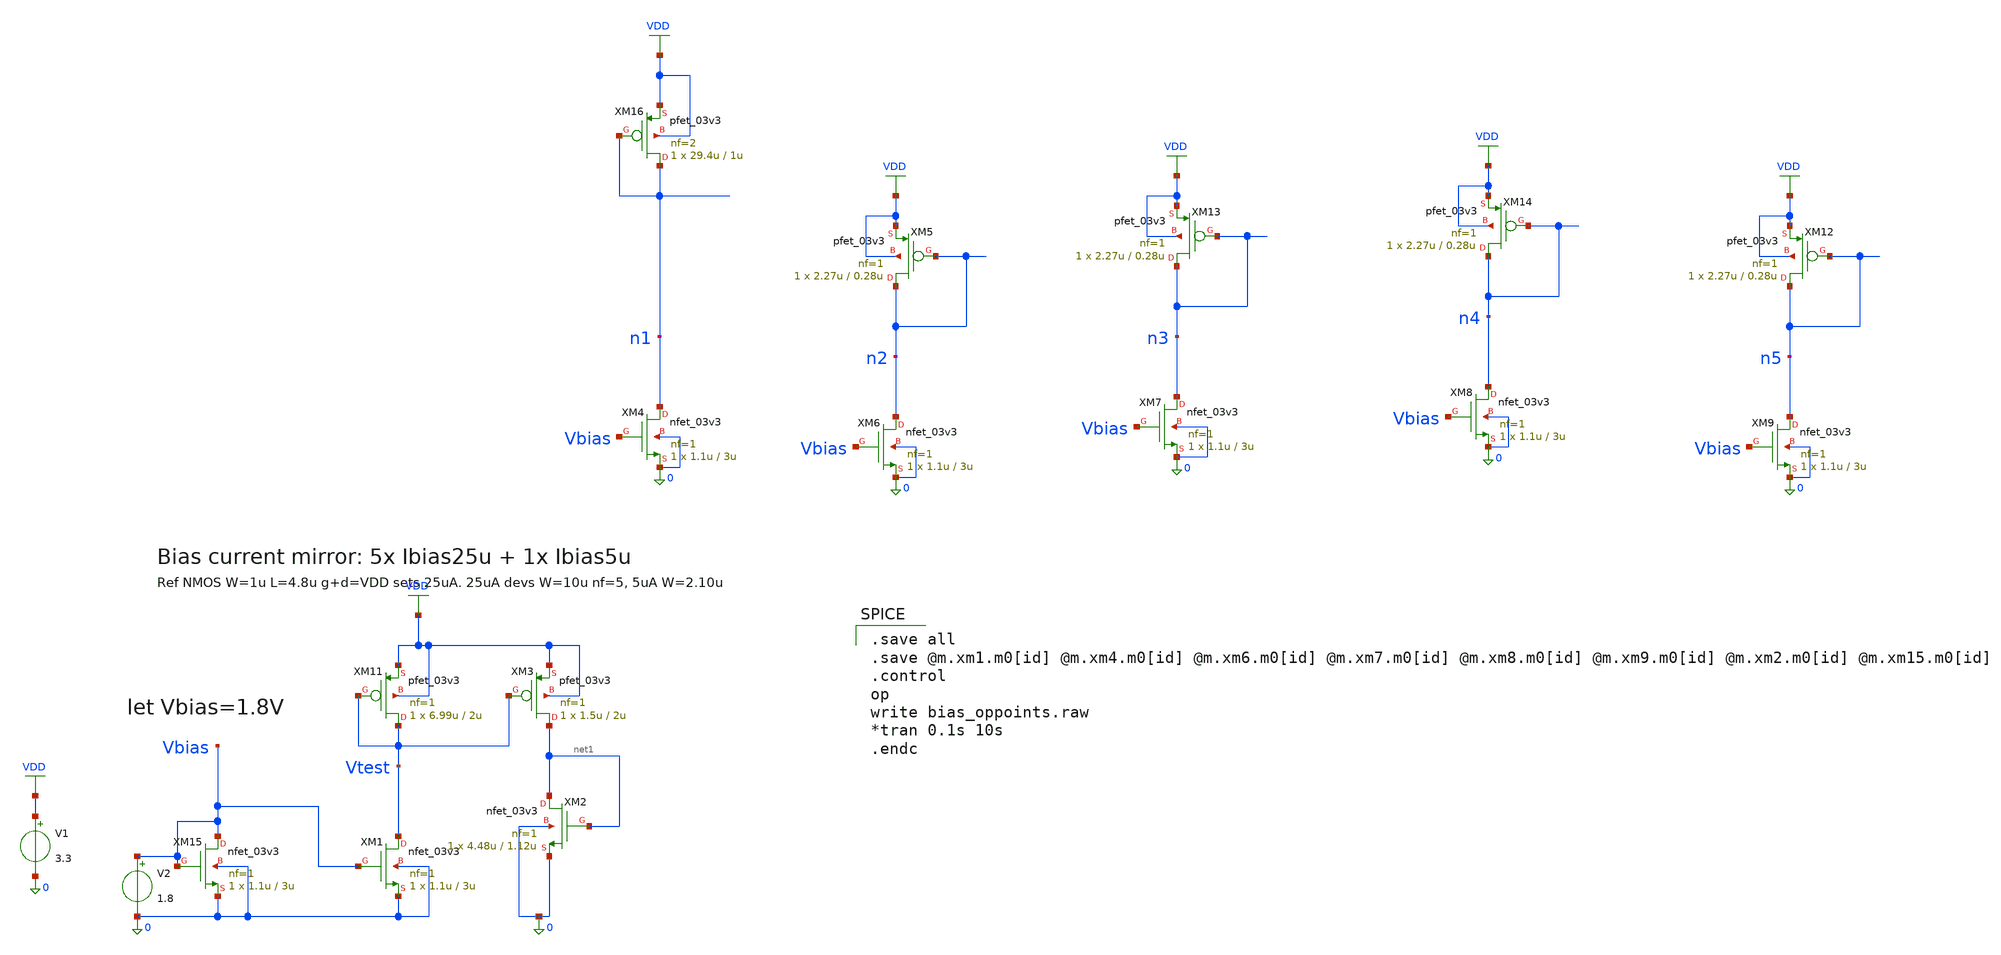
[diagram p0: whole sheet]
** sch_path: ps-bias/jz_bias_tb.sch
**.subckt jz_bias_tb
V1 VDD 0 3.3
V2 Vbias 0 1.8
XM5 n2 n2 VDD VDD pfet_03v3 L=0.28u W=2.27u nf=1 ad='int((nf+1)/2) * W/nf * 0.18u' as='int((nf+2)/2) * W/nf * 0.18u'
+ pd='2*int((nf+1)/2) * (W/nf + 0.18u)' ps='2*int((nf+2)/2) * (W/nf + 0.18u)' nrd='0.18u / W' nrs='0.18u / W'
+ sa=0 sb=0 sd=0 m=1
XM13 n3 n3 VDD VDD pfet_03v3 L=0.28u W=2.27u nf=1 ad='int((nf+1)/2) * W/nf * 0.18u' as='int((nf+2)/2) * W/nf * 0.18u'
+ pd='2*int((nf+1)/2) * (W/nf + 0.18u)' ps='2*int((nf+2)/2) * (W/nf + 0.18u)' nrd='0.18u / W' nrs='0.18u / W'
+ sa=0 sb=0 sd=0 m=1
XM14 n4 n4 VDD VDD pfet_03v3 L=0.28u W=2.27u nf=1 ad='int((nf+1)/2) * W/nf * 0.18u' as='int((nf+2)/2) * W/nf * 0.18u'
+ pd='2*int((nf+1)/2) * (W/nf + 0.18u)' ps='2*int((nf+2)/2) * (W/nf + 0.18u)' nrd='0.18u / W' nrs='0.18u / W'
+ sa=0 sb=0 sd=0 m=1
XM12 n5 n5 VDD VDD pfet_03v3 L=0.28u W=2.27u nf=1 ad='int((nf+1)/2) * W/nf * 0.18u' as='int((nf+2)/2) * W/nf * 0.18u'
+ pd='2*int((nf+1)/2) * (W/nf + 0.18u)' ps='2*int((nf+2)/2) * (W/nf + 0.18u)' nrd='0.18u / W' nrs='0.18u / W'
+ sa=0 sb=0 sd=0 m=1
XM15 Vbias Vbias 0 0 nfet_03v3 L=3u W=1.1u nf=1 ad='int((nf+1)/2) * W/nf * 0.18u' as='int((nf+2)/2) * W/nf * 0.18u'
+ pd='2*int((nf+1)/2) * (W/nf + 0.18u)' ps='2*int((nf+2)/2) * (W/nf + 0.18u)' nrd='0.18u / W' nrs='0.18u / W'
+ sa=0 sb=0 sd=0 m=1
XM1 Vtest Vbias 0 0 nfet_03v3 L=3u W=1.1u nf=1 ad='int((nf+1)/2) * W/nf * 0.18u' as='int((nf+2)/2) * W/nf * 0.18u'
+ pd='2*int((nf+1)/2) * (W/nf + 0.18u)' ps='2*int((nf+2)/2) * (W/nf + 0.18u)' nrd='0.18u / W' nrs='0.18u / W'
+ sa=0 sb=0 sd=0 m=1
XM4 n1 Vbias 0 0 nfet_03v3 L=3u W=1.1u nf=1 ad='int((nf+1)/2) * W/nf * 0.18u' as='int((nf+2)/2) * W/nf * 0.18u'
+ pd='2*int((nf+1)/2) * (W/nf + 0.18u)' ps='2*int((nf+2)/2) * (W/nf + 0.18u)' nrd='0.18u / W' nrs='0.18u / W'
+ sa=0 sb=0 sd=0 m=1
XM6 n2 Vbias 0 0 nfet_03v3 L=3u W=1.1u nf=1 ad='int((nf+1)/2) * W/nf * 0.18u' as='int((nf+2)/2) * W/nf * 0.18u'
+ pd='2*int((nf+1)/2) * (W/nf + 0.18u)' ps='2*int((nf+2)/2) * (W/nf + 0.18u)' nrd='0.18u / W' nrs='0.18u / W'
+ sa=0 sb=0 sd=0 m=1
XM7 n3 Vbias 0 0 nfet_03v3 L=3u W=1.1u nf=1 ad='int((nf+1)/2) * W/nf * 0.18u' as='int((nf+2)/2) * W/nf * 0.18u'
+ pd='2*int((nf+1)/2) * (W/nf + 0.18u)' ps='2*int((nf+2)/2) * (W/nf + 0.18u)' nrd='0.18u / W' nrs='0.18u / W'
+ sa=0 sb=0 sd=0 m=1
XM8 n4 Vbias 0 0 nfet_03v3 L=3u W=1.1u nf=1 ad='int((nf+1)/2) * W/nf * 0.18u' as='int((nf+2)/2) * W/nf * 0.18u'
+ pd='2*int((nf+1)/2) * (W/nf + 0.18u)' ps='2*int((nf+2)/2) * (W/nf + 0.18u)' nrd='0.18u / W' nrs='0.18u / W'
+ sa=0 sb=0 sd=0 m=1
XM9 n5 Vbias 0 0 nfet_03v3 L=3u W=1.1u nf=1 ad='int((nf+1)/2) * W/nf * 0.18u' as='int((nf+2)/2) * W/nf * 0.18u'
+ pd='2*int((nf+1)/2) * (W/nf + 0.18u)' ps='2*int((nf+2)/2) * (W/nf + 0.18u)' nrd='0.18u / W' nrs='0.18u / W'
+ sa=0 sb=0 sd=0 m=1
XM11 Vtest Vtest VDD VDD pfet_03v3 L=2u W=6.99u nf=1 ad='int((nf+1)/2) * W/nf * 0.18u' as='int((nf+2)/2) * W/nf * 0.18u'
+ pd='2*int((nf+1)/2) * (W/nf + 0.18u)' ps='2*int((nf+2)/2) * (W/nf + 0.18u)' nrd='0.18u / W' nrs='0.18u / W'
+ sa=0 sb=0 sd=0 m=1
XM3 net1 Vtest VDD VDD pfet_03v3 L=2u W=1.5u nf=1 ad='int((nf+1)/2) * W/nf * 0.18u' as='int((nf+2)/2) * W/nf * 0.18u'
+ pd='2*int((nf+1)/2) * (W/nf + 0.18u)' ps='2*int((nf+2)/2) * (W/nf + 0.18u)' nrd='0.18u / W' nrs='0.18u / W'
+ sa=0 sb=0 sd=0 m=1
XM2 net1 net1 0 0 nfet_03v3 L=1.12u W=4.48u nf=1 ad='int((nf+1)/2) * W/nf * 0.18u' as='int((nf+2)/2) * W/nf * 0.18u'
+ pd='2*int((nf+1)/2) * (W/nf + 0.18u)' ps='2*int((nf+2)/2) * (W/nf + 0.18u)' nrd='0.18u / W' nrs='0.18u / W'
+ sa=0 sb=0 sd=0 m=1
XM16 n1 n1 VDD VDD pfet_03v3 L=1u W=29.4u nf=2 ad='int((nf+1)/2) * W/nf * 0.18u' as='int((nf+2)/2) * W/nf * 0.18u'
+ pd='2*int((nf+1)/2) * (W/nf + 0.18u)' ps='2*int((nf+2)/2) * (W/nf + 0.18u)' nrd='0.18u / W' nrs='0.18u / W'
+ sa=0 sb=0 sd=0 m=1
**** begin user architecture code

.save all
.save @m.xm1.m0[id] @m.xm4.m0[id] @m.xm6.m0[id] @m.xm7.m0[id] @m.xm8.m0[id] @m.xm9.m0[id] @m.xm2.m0[id] @m.xm15.m0[id]
.control
op
write bias_oppoints.raw
*tran 0.1s 10s
.endc


.include $::180MCU_MODELS/design.ngspice
.lib $::180MCU_MODELS/sm141064.ngspice typical
.lib $::180MCU_MODELS/smbb000149.ngspice typical

**** end user architecture code
**.ends
.GLOBAL VDD
.end
